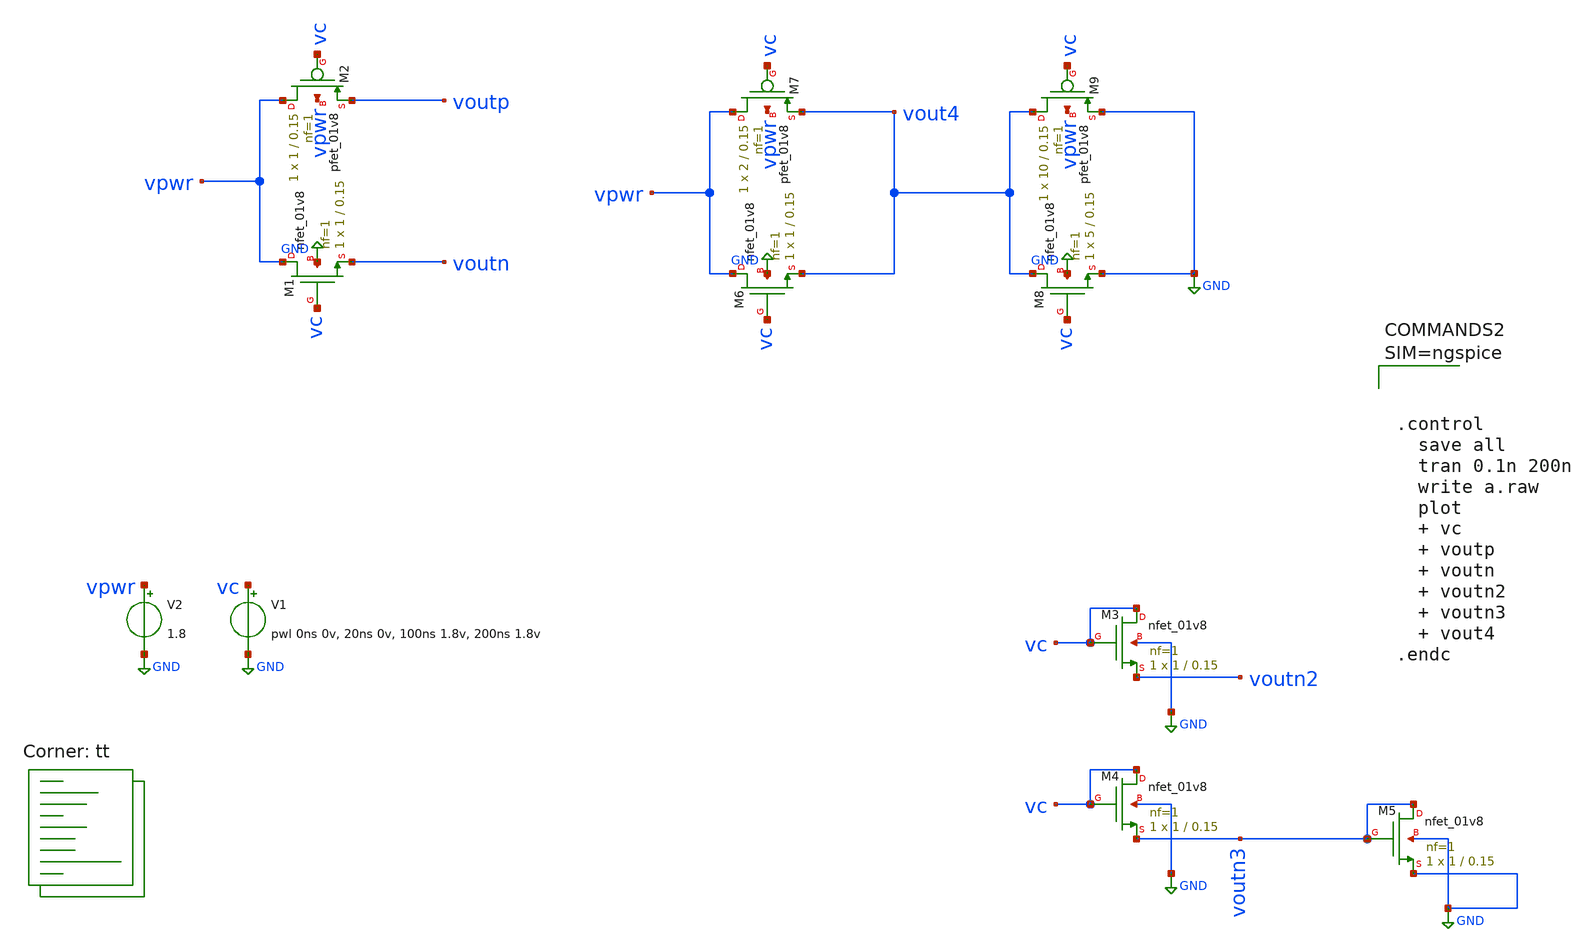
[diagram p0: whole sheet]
** sch_path: xschem/a.sch
**.subckt a
XM1 vpwr vc voutn GND sky130_fd_pr__nfet_01v8 L=0.15 W=1 nf=1 ad='int((nf+1)/2) * W/nf * 0.29' as='int((nf+2)/2) * W/nf * 0.29'
+ pd='2*int((nf+1)/2) * (W/nf + 0.29)' ps='2*int((nf+2)/2) * (W/nf + 0.29)' nrd='0.29 / W' nrs='0.29 / W'
+ sa=0 sb=0 sd=0 mult=1 m=1
V1 vc GND pwl 0ns 0v, 20ns 0v, 100ns 1.8v, 200ns 1.8v
XM2 vpwr vc voutp vpwr sky130_fd_pr__pfet_01v8 L=0.15 W=1 nf=1 ad='int((nf+1)/2) * W/nf * 0.29' as='int((nf+2)/2) * W/nf * 0.29'
+ pd='2*int((nf+1)/2) * (W/nf + 0.29)' ps='2*int((nf+2)/2) * (W/nf + 0.29)' nrd='0.29 / W' nrs='0.29 / W'
+ sa=0 sb=0 sd=0 mult=1 m=1
V2 vpwr GND 1.8
XM3 vc vc voutn2 GND sky130_fd_pr__nfet_01v8 L=0.15 W=1 nf=1 ad='int((nf+1)/2) * W/nf * 0.29' as='int((nf+2)/2) * W/nf * 0.29'
+ pd='2*int((nf+1)/2) * (W/nf + 0.29)' ps='2*int((nf+2)/2) * (W/nf + 0.29)' nrd='0.29 / W' nrs='0.29 / W'
+ sa=0 sb=0 sd=0 mult=1 m=1
XM4 vc vc voutn3 GND sky130_fd_pr__nfet_01v8 L=0.15 W=1 nf=1 ad='int((nf+1)/2) * W/nf * 0.29' as='int((nf+2)/2) * W/nf * 0.29'
+ pd='2*int((nf+1)/2) * (W/nf + 0.29)' ps='2*int((nf+2)/2) * (W/nf + 0.29)' nrd='0.29 / W' nrs='0.29 / W'
+ sa=0 sb=0 sd=0 mult=1 m=1
XM5 voutn3 voutn3 GND GND sky130_fd_pr__nfet_01v8 L=0.15 W=1 nf=1 ad='int((nf+1)/2) * W/nf * 0.29' as='int((nf+2)/2) * W/nf * 0.29'
+ pd='2*int((nf+1)/2) * (W/nf + 0.29)' ps='2*int((nf+2)/2) * (W/nf + 0.29)' nrd='0.29 / W' nrs='0.29 / W'
+ sa=0 sb=0 sd=0 mult=1 m=1
XM6 vpwr vc vout4 GND sky130_fd_pr__nfet_01v8 L=0.15 W=1 nf=1 ad='int((nf+1)/2) * W/nf * 0.29' as='int((nf+2)/2) * W/nf * 0.29'
+ pd='2*int((nf+1)/2) * (W/nf + 0.29)' ps='2*int((nf+2)/2) * (W/nf + 0.29)' nrd='0.29 / W' nrs='0.29 / W'
+ sa=0 sb=0 sd=0 mult=1 m=1
XM7 vpwr vc vout4 vpwr sky130_fd_pr__pfet_01v8 L=0.15 W=2 nf=1 ad='int((nf+1)/2) * W/nf * 0.29' as='int((nf+2)/2) * W/nf * 0.29'
+ pd='2*int((nf+1)/2) * (W/nf + 0.29)' ps='2*int((nf+2)/2) * (W/nf + 0.29)' nrd='0.29 / W' nrs='0.29 / W'
+ sa=0 sb=0 sd=0 mult=1 m=1
XM8 vout4 vc GND GND sky130_fd_pr__nfet_01v8 L=0.15 W=5 nf=1 ad='int((nf+1)/2) * W/nf * 0.29' as='int((nf+2)/2) * W/nf * 0.29'
+ pd='2*int((nf+1)/2) * (W/nf + 0.29)' ps='2*int((nf+2)/2) * (W/nf + 0.29)' nrd='0.29 / W' nrs='0.29 / W'
+ sa=0 sb=0 sd=0 mult=1 m=1
XM9 vout4 vc GND vpwr sky130_fd_pr__pfet_01v8 L=0.15 W=10 nf=1 ad='int((nf+1)/2) * W/nf * 0.29' as='int((nf+2)/2) * W/nf * 0.29'
+ pd='2*int((nf+1)/2) * (W/nf + 0.29)' ps='2*int((nf+2)/2) * (W/nf + 0.29)' nrd='0.29 / W' nrs='0.29 / W'
+ sa=0 sb=0 sd=0 mult=1 m=1
**** begin user architecture code
.lib $::SKYWATER_MODELS/sky130.lib.spice tt




.control
  save all
  tran 0.1n 200n
  write a.raw
  plot
  + vc
  + voutp
  + voutn
  + voutn2
  + voutn3
  + vout4
.endc




**** end user architecture code
**.ends
.GLOBAL GND
.end
